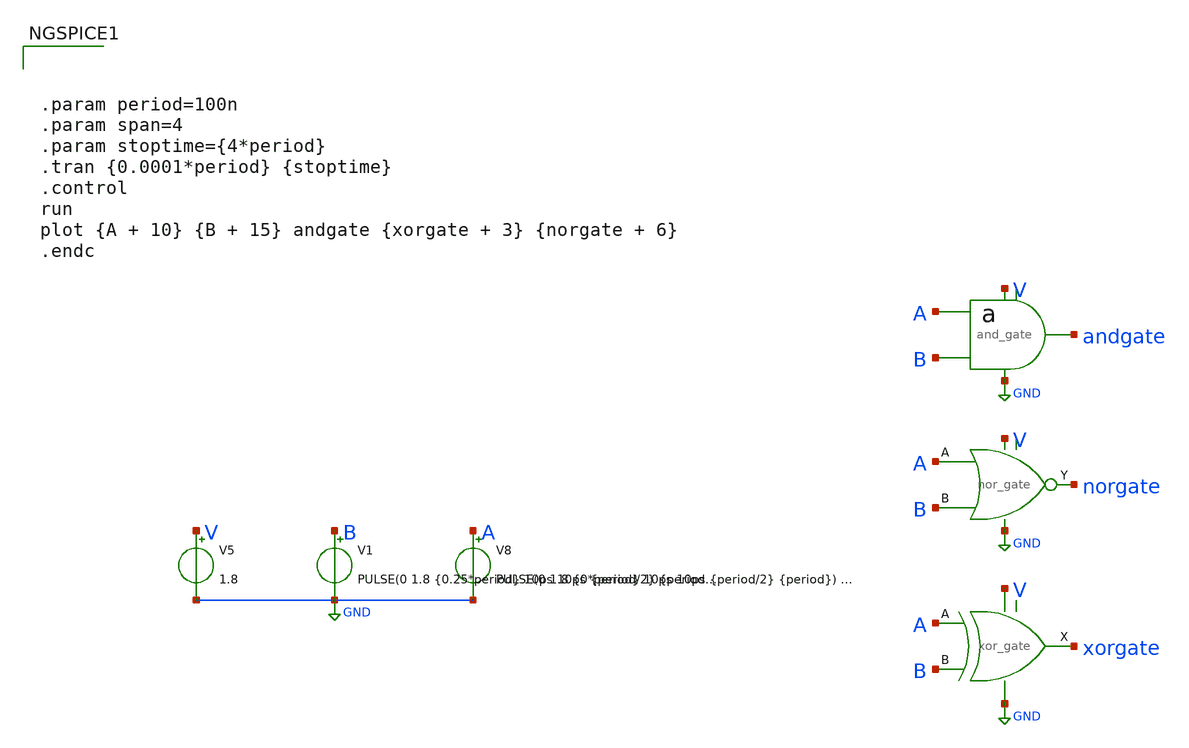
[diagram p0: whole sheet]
** sch_path: xschem/designs/counter4b/int_gate_tb.sch
* xschem/designs/counter4b/and_gate.sym:
* Copyright 2022 Stefan Frederik Schippers
* Licensed under the Apache License, Version 2.0 (the "License");
**.subckt int_gate_tb
V5 V GND 1.8
V8 A GND PULSE(0 1.8 {0*period} 10ps 10ps {period/2} {period}) DC 0
V1 B GND PULSE(0 1.8 {0.25*period} 10ps 10ps {period/2} {period}) DC 0
X1 A B GND V andgate and_gate
X2 norgate B A V GND nor_gate
X3 A B xorgate V GND xor_gate
**** begin user architecture code



.param period=100n
.param span=4
.param stoptime={4*period}
.tran {0.0001*period} {stoptime}
.control
run
plot {A + 10} {B + 15} andgate {xorgate + 3} {norgate + 6}
.endc



.lib $env(PDK_ROOT)/$env(PDK)/libs.tech/ngspice/sky130.lib.spice.tt.red tt


**** end user architecture code
**.ends

* expanding   symbol:  /foss/designs/EAMTA2024/EAMTA/xschem/counter4b/symbol/and_gate.sym # of
*+ pins=5
** sym_path: xschem/designs/counter4b/and_gate.sym
** sch_path: xschem/designs/counter4b/and_gate.sch
.subckt and_gate A B gnd V out
*.iopin A
*.iopin out
*.iopin gnd
*.iopin V
*.iopin B
XM1 gnd A net2 gnd sky130_fd_pr__nfet_01v8 L=0.15 W=1.5 nf=1 ad='int((nf+1)/2) * W/nf * 0.29' as='int((nf+2)/2) * W/nf * 0.29'
+ pd='2*int((nf+1)/2) * (W/nf + 0.29)' ps='2*int((nf+2)/2) * (W/nf + 0.29)' nrd='0.29 / W' nrs='0.29 / W'
+ sa=0 sb=0 sd=0 mult=1 m=1
XM2 net1 A V V sky130_fd_pr__pfet_01v8 L=0.15 W=1.5 nf=1 ad='int((nf+1)/2) * W/nf * 0.29' as='int((nf+2)/2) * W/nf * 0.29'
+ pd='2*int((nf+1)/2) * (W/nf + 0.29)' ps='2*int((nf+2)/2) * (W/nf + 0.29)' nrd='0.29 / W' nrs='0.29 / W'
+ sa=0 sb=0 sd=0 mult=1 m=1
XM3 net1 B net2 gnd sky130_fd_pr__nfet_01v8 L=0.15 W=1.5 nf=1 ad='int((nf+1)/2) * W/nf * 0.29' as='int((nf+2)/2) * W/nf * 0.29'
+ pd='2*int((nf+1)/2) * (W/nf + 0.29)' ps='2*int((nf+2)/2) * (W/nf + 0.29)' nrd='0.29 / W' nrs='0.29 / W'
+ sa=0 sb=0 sd=0 mult=1 m=1
XM4 net1 B V V sky130_fd_pr__pfet_01v8 L=0.15 W=1.5 nf=1 ad='int((nf+1)/2) * W/nf * 0.29' as='int((nf+2)/2) * W/nf * 0.29'
+ pd='2*int((nf+1)/2) * (W/nf + 0.29)' ps='2*int((nf+2)/2) * (W/nf + 0.29)' nrd='0.29 / W' nrs='0.29 / W'
+ sa=0 sb=0 sd=0 mult=1 m=1
X1 V gnd net1 out inv_gate
.ends


* expanding   symbol:  /foss/designs/EAMTA2024/EAMTA/xschem/counter4b/symbol/nor_gate.sym # of
*+ pins=5
** sym_path: xschem/designs/counter4b/nor_gate.sym
** sch_path: xschem/designs/counter4b/nor_gate.sch
.subckt nor_gate out B A V gnd
*.iopin A
*.iopin out
*.iopin gnd
*.iopin V
*.iopin B
XM1 out A gnd gnd sky130_fd_pr__nfet_01v8 L=0.15 W=0.75 nf=1 ad='int((nf+1)/2) * W/nf * 0.29' as='int((nf+2)/2) * W/nf * 0.29'
+ pd='2*int((nf+1)/2) * (W/nf + 0.29)' ps='2*int((nf+2)/2) * (W/nf + 0.29)' nrd='0.29 / W' nrs='0.29 / W'
+ sa=0 sb=0 sd=0 mult=1 m=1
XM2 net1 A V V sky130_fd_pr__pfet_01v8 L=0.15 W=3 nf=1 ad='int((nf+1)/2) * W/nf * 0.29' as='int((nf+2)/2) * W/nf * 0.29'
+ pd='2*int((nf+1)/2) * (W/nf + 0.29)' ps='2*int((nf+2)/2) * (W/nf + 0.29)' nrd='0.29 / W' nrs='0.29 / W'
+ sa=0 sb=0 sd=0 mult=1 m=1
XM3 out B gnd gnd sky130_fd_pr__nfet_01v8 L=0.15 W=0.75 nf=1 ad='int((nf+1)/2) * W/nf * 0.29' as='int((nf+2)/2) * W/nf * 0.29'
+ pd='2*int((nf+1)/2) * (W/nf + 0.29)' ps='2*int((nf+2)/2) * (W/nf + 0.29)' nrd='0.29 / W' nrs='0.29 / W'
+ sa=0 sb=0 sd=0 mult=1 m=1
XM4 out B net1 V sky130_fd_pr__pfet_01v8 L=0.15 W=3 nf=1 ad='int((nf+1)/2) * W/nf * 0.29' as='int((nf+2)/2) * W/nf * 0.29'
+ pd='2*int((nf+1)/2) * (W/nf + 0.29)' ps='2*int((nf+2)/2) * (W/nf + 0.29)' nrd='0.29 / W' nrs='0.29 / W'
+ sa=0 sb=0 sd=0 mult=1 m=1
.ends


* expanding   symbol:  /foss/designs/EAMTA2024/EAMTA/xschem/counter4b/symbol/xor_gate.sym # of
*+ pins=5
** sym_path: xschem/designs/counter4b/xor_gate.sym
** sch_path: xschem/designs/counter4b/xor_gate.sch
.subckt xor_gate A B out V gnd
*.iopin A
*.iopin out
*.iopin gnd
*.iopin V
*.iopin B
XM1 out B net3 gnd sky130_fd_pr__nfet_01v8 L=0.15 W=1.5 nf=1 ad='int((nf+1)/2) * W/nf * 0.29' as='int((nf+2)/2) * W/nf * 0.29'
+ pd='2*int((nf+1)/2) * (W/nf + 0.29)' ps='2*int((nf+2)/2) * (W/nf + 0.29)' nrd='0.29 / W' nrs='0.29 / W'
+ sa=0 sb=0 sd=0 mult=1 m=1
XM2 net1 A V V sky130_fd_pr__pfet_01v8 L=0.15 W=1.5 nf=1 ad='int((nf+1)/2) * W/nf * 0.29' as='int((nf+2)/2) * W/nf * 0.29'
+ pd='2*int((nf+1)/2) * (W/nf + 0.29)' ps='2*int((nf+2)/2) * (W/nf + 0.29)' nrd='0.29 / W' nrs='0.29 / W'
+ sa=0 sb=0 sd=0 mult=1 m=1
XM3 gnd A net3 gnd sky130_fd_pr__nfet_01v8 L=0.15 W=1.5 nf=1 ad='int((nf+1)/2) * W/nf * 0.29' as='int((nf+2)/2) * W/nf * 0.29'
+ pd='2*int((nf+1)/2) * (W/nf + 0.29)' ps='2*int((nf+2)/2) * (W/nf + 0.29)' nrd='0.29 / W' nrs='0.29 / W'
+ sa=0 sb=0 sd=0 mult=1 m=1
XM4 out nB net1 V sky130_fd_pr__pfet_01v8 L=0.15 W=1.5 nf=1 ad='int((nf+1)/2) * W/nf * 0.29' as='int((nf+2)/2) * W/nf * 0.29'
+ pd='2*int((nf+1)/2) * (W/nf + 0.29)' ps='2*int((nf+2)/2) * (W/nf + 0.29)' nrd='0.29 / W' nrs='0.29 / W'
+ sa=0 sb=0 sd=0 mult=1 m=1
XM5 net1 B V V sky130_fd_pr__pfet_01v8 L=0.15 W=1.5 nf=1 ad='int((nf+1)/2) * W/nf * 0.29' as='int((nf+2)/2) * W/nf * 0.29'
+ pd='2*int((nf+1)/2) * (W/nf + 0.29)' ps='2*int((nf+2)/2) * (W/nf + 0.29)' nrd='0.29 / W' nrs='0.29 / W'
+ sa=0 sb=0 sd=0 mult=1 m=1
XM6 out nA net1 V sky130_fd_pr__pfet_01v8 L=0.15 W=1.5 nf=1 ad='int((nf+1)/2) * W/nf * 0.29' as='int((nf+2)/2) * W/nf * 0.29'
+ pd='2*int((nf+1)/2) * (W/nf + 0.29)' ps='2*int((nf+2)/2) * (W/nf + 0.29)' nrd='0.29 / W' nrs='0.29 / W'
+ sa=0 sb=0 sd=0 mult=1 m=1
XM7 out nA net2 gnd sky130_fd_pr__nfet_01v8 L=0.15 W=1.5 nf=1 ad='int((nf+1)/2) * W/nf * 0.29' as='int((nf+2)/2) * W/nf * 0.29'
+ pd='2*int((nf+1)/2) * (W/nf + 0.29)' ps='2*int((nf+2)/2) * (W/nf + 0.29)' nrd='0.29 / W' nrs='0.29 / W'
+ sa=0 sb=0 sd=0 mult=1 m=1
XM8 gnd nB net2 gnd sky130_fd_pr__nfet_01v8 L=0.15 W=1.5 nf=1 ad='int((nf+1)/2) * W/nf * 0.29' as='int((nf+2)/2) * W/nf * 0.29'
+ pd='2*int((nf+1)/2) * (W/nf + 0.29)' ps='2*int((nf+2)/2) * (W/nf + 0.29)' nrd='0.29 / W' nrs='0.29 / W'
+ sa=0 sb=0 sd=0 mult=1 m=1
XM9 nA A V V sky130_fd_pr__pfet_01v8 L=0.15 W=1.5 nf=1 ad='int((nf+1)/2) * W/nf * 0.29' as='int((nf+2)/2) * W/nf * 0.29'
+ pd='2*int((nf+1)/2) * (W/nf + 0.29)' ps='2*int((nf+2)/2) * (W/nf + 0.29)' nrd='0.29 / W' nrs='0.29 / W'
+ sa=0 sb=0 sd=0 mult=1 m=1
XM10 nA A gnd gnd sky130_fd_pr__nfet_01v8 L=0.15 W=0.75 nf=1 ad='int((nf+1)/2) * W/nf * 0.29' as='int((nf+2)/2) * W/nf * 0.29'
+ pd='2*int((nf+1)/2) * (W/nf + 0.29)' ps='2*int((nf+2)/2) * (W/nf + 0.29)' nrd='0.29 / W' nrs='0.29 / W'
+ sa=0 sb=0 sd=0 mult=1 m=1
XM11 nB B V V sky130_fd_pr__pfet_01v8 L=0.15 W=1.5 nf=1 ad='int((nf+1)/2) * W/nf * 0.29' as='int((nf+2)/2) * W/nf * 0.29'
+ pd='2*int((nf+1)/2) * (W/nf + 0.29)' ps='2*int((nf+2)/2) * (W/nf + 0.29)' nrd='0.29 / W' nrs='0.29 / W'
+ sa=0 sb=0 sd=0 mult=1 m=1
XM12 nB B gnd gnd sky130_fd_pr__nfet_01v8 L=0.15 W=0.75 nf=1 ad='int((nf+1)/2) * W/nf * 0.29' as='int((nf+2)/2) * W/nf * 0.29'
+ pd='2*int((nf+1)/2) * (W/nf + 0.29)' ps='2*int((nf+2)/2) * (W/nf + 0.29)' nrd='0.29 / W' nrs='0.29 / W'
+ sa=0 sb=0 sd=0 mult=1 m=1
.ends


* expanding   symbol:  inv_gate.sym # of pins=4
** sym_path: xschem/designs/counter4b/inv_gate.sym
** sch_path: xschem/designs/counter4b/inv_gate.sch
.subckt inv_gate V gnd in out
*.iopin in
*.iopin out
*.iopin gnd
*.iopin V
XM1 out in gnd gnd sky130_fd_pr__nfet_01v8 L=0.15 W=0.75 nf=1 ad='int((nf+1)/2) * W/nf * 0.29' as='int((nf+2)/2) * W/nf * 0.29'
+ pd='2*int((nf+1)/2) * (W/nf + 0.29)' ps='2*int((nf+2)/2) * (W/nf + 0.29)' nrd='0.29 / W' nrs='0.29 / W'
+ sa=0 sb=0 sd=0 mult=1 m=1
XM2 out in V V sky130_fd_pr__pfet_01v8 L=0.15 W=1.5 nf=1 ad='int((nf+1)/2) * W/nf * 0.29' as='int((nf+2)/2) * W/nf * 0.29'
+ pd='2*int((nf+1)/2) * (W/nf + 0.29)' ps='2*int((nf+2)/2) * (W/nf + 0.29)' nrd='0.29 / W' nrs='0.29 / W'
+ sa=0 sb=0 sd=0 mult=1 m=1
.ends

.GLOBAL GND
.end
